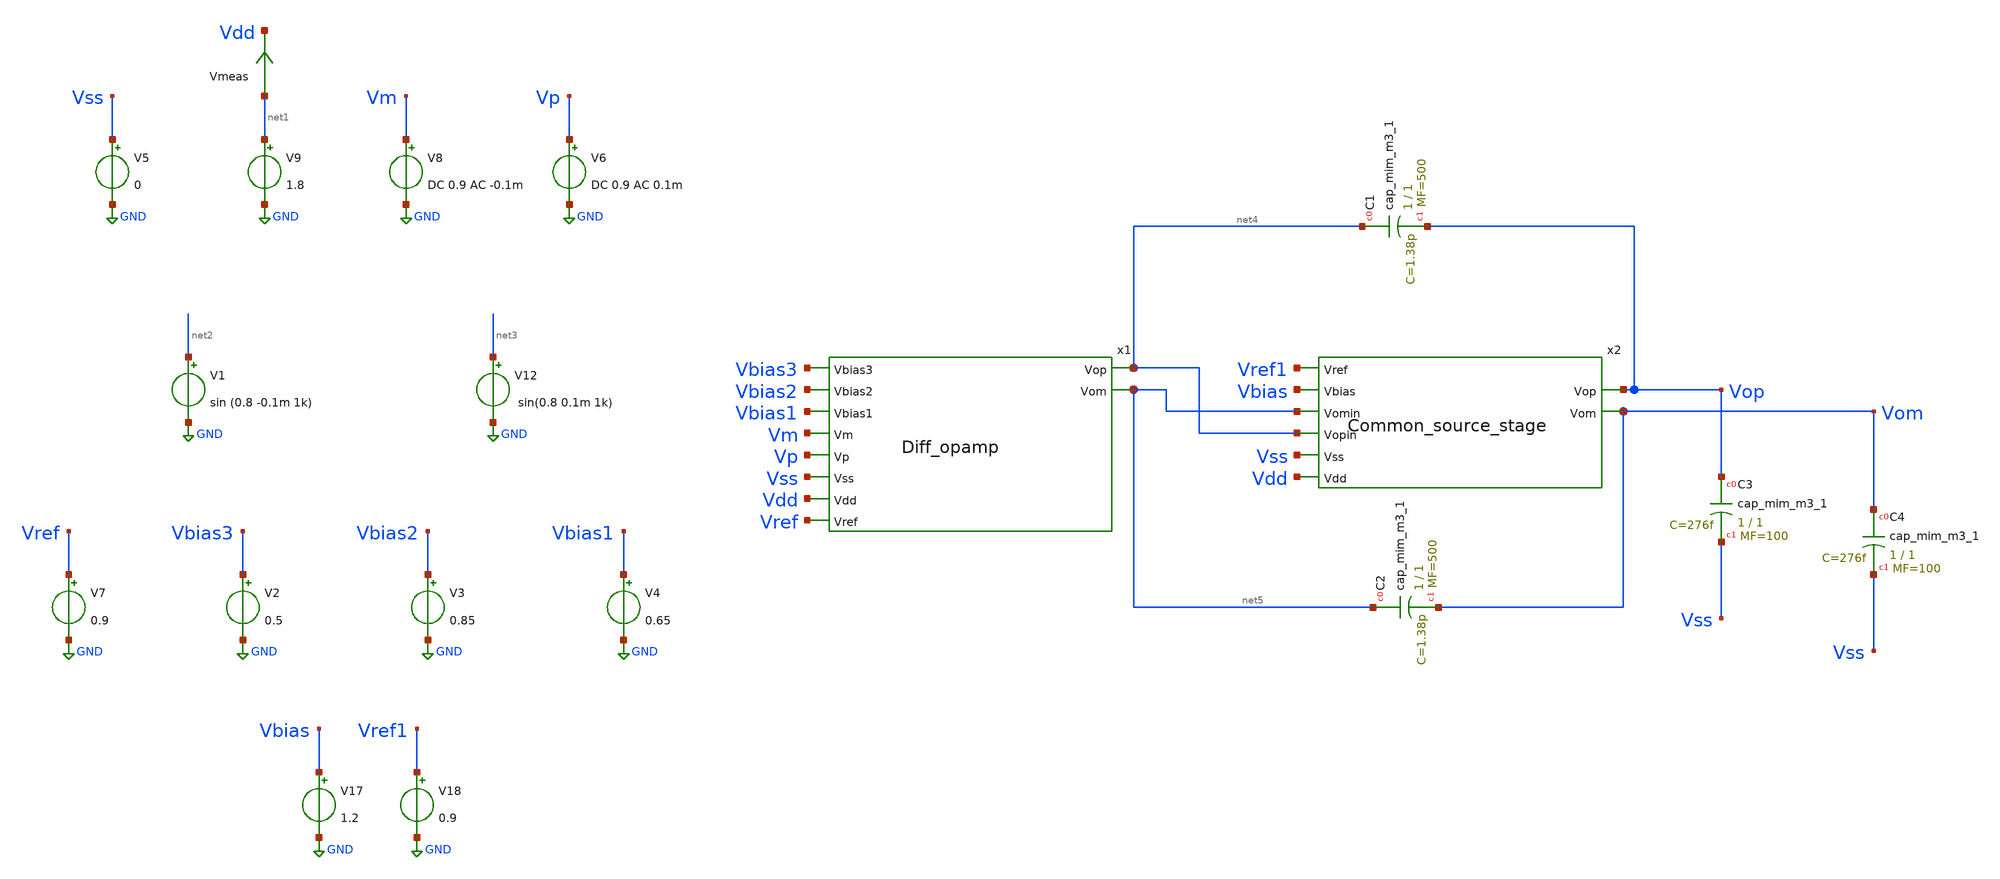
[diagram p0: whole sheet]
** sch_path: src/Opamp_Design/testbenches/OpAmp_top_tb.sch
**.subckt OpAmp_top_tb
x1 Vbias3 Vbias2 Vbias1 Vm Vp Vss Vdd Vref net4 net5 Diff_opamp
x2 Vref1 Vbias net5 net4 Vss Vdd Vop Vom Common_source_stage
V8 Vm GND DC 0.9 AC -0.1m
V6 Vp GND DC 0.9 AC 0.1m
V9 net1 GND 1.8
Vmeas net1 Vdd 0
.save i(vmeas)
V1 net2 GND sin (0.8 -0.1m 1k)
V12 net3 GND sin(0.8 0.1m 1k)
V2 Vbias3 GND 0.5
V3 Vbias2 GND 0.85
V4 Vbias1 GND 0.65
V5 Vss GND 0
V7 Vref GND 0.9
V17 Vbias GND 1.2
V18 Vref1 GND 0.9
XC1 net4 Vop sky130_fd_pr__cap_mim_m3_1 W=1 L=1 MF=500 m=500
XC3 Vop Vss sky130_fd_pr__cap_mim_m3_1 W=1 L=1 MF=100 m=100
XC4 Vom Vss sky130_fd_pr__cap_mim_m3_1 W=1 L=1 MF=100 m=100
XC2 net5 Vom sky130_fd_pr__cap_mim_m3_1 W=1 L=1 MF=500 m=500
**** begin user architecture code

** opencircuitdesign pdks install
.lib $::SKYWATER_MODELS/sky130.lib.spice tt


**** end user architecture code
**.ends

* expanding   symbol:  /foss/designs/FYP/Sky130_Multiplier/Opamp_Design/src/Diff_opamp.sym # of
*+ pins=10
** sym_path: src/Opamp_Design/src/Diff_opamp.sym
** sch_path: src/Opamp_Design/src/Diff_opamp.sch
.subckt Diff_opamp Vbias3 Vbias2 Vbias1 Vm Vp Vss Vdd Vref Vop Vom
*.ipin Vss
*.opin Vop
*.ipin Vdd
*.ipin Vp
*.ipin Vm
*.ipin Vref
*.opin Vom
*.ipin Vbias1
*.ipin Vbias2
*.ipin Vbias3
XM5 Vtest2 Vm net2 Vss sky130_fd_pr__nfet_01v8_lvt L=4 W=4 nf=1 ad='int((nf+1)/2) * W/nf * 0.29' as='int((nf+2)/2) * W/nf * 0.29'
+ pd='2*int((nf+1)/2) * (W/nf + 0.29)' ps='2*int((nf+2)/2) * (W/nf + 0.29)' nrd='0.29 / W' nrs='0.29 / W'
+ sa=0 sb=0 sd=0 mult=2 m=2
XM6 net1 Vp net2 Vss sky130_fd_pr__nfet_01v8_lvt L=4 W=4 nf=1 ad='int((nf+1)/2) * W/nf * 0.29' as='int((nf+2)/2) * W/nf * 0.29'
+ pd='2*int((nf+1)/2) * (W/nf + 0.29)' ps='2*int((nf+2)/2) * (W/nf + 0.29)' nrd='0.29 / W' nrs='0.29 / W'
+ sa=0 sb=0 sd=0 mult=2 m=2
XM11 Vop Vbias Vtest2 Vdd sky130_fd_pr__pfet_01v8_lvt L=5 W=2 nf=1 ad='int((nf+1)/2) * W/nf * 0.29' as='int((nf+2)/2) * W/nf * 0.29'
+ pd='2*int((nf+1)/2) * (W/nf + 0.29)' ps='2*int((nf+2)/2) * (W/nf + 0.29)' nrd='0.29 / W' nrs='0.29 / W'
+ sa=0 sb=0 sd=0 mult=2 m=2
XM12 Vom Vbias net1 Vdd sky130_fd_pr__pfet_01v8_lvt L=5 W=2 nf=1 ad='int((nf+1)/2) * W/nf * 0.29' as='int((nf+2)/2) * W/nf * 0.29'
+ pd='2*int((nf+1)/2) * (W/nf + 0.29)' ps='2*int((nf+2)/2) * (W/nf + 0.29)' nrd='0.29 / W' nrs='0.29 / W'
+ sa=0 sb=0 sd=0 mult=2 m=2
XM13 Vtest2 Vout Vdd Vdd sky130_fd_pr__pfet_01v8_lvt L=5 W=2 nf=1 ad='int((nf+1)/2) * W/nf * 0.29' as='int((nf+2)/2) * W/nf * 0.29'
+ pd='2*int((nf+1)/2) * (W/nf + 0.29)' ps='2*int((nf+2)/2) * (W/nf + 0.29)' nrd='0.29 / W' nrs='0.29 / W'
+ sa=0 sb=0 sd=0 mult=4 m=4
XM14 net1 Vout Vdd Vdd sky130_fd_pr__pfet_01v8_lvt L=5 W=2 nf=1 ad='int((nf+1)/2) * W/nf * 0.29' as='int((nf+2)/2) * W/nf * 0.29'
+ pd='2*int((nf+1)/2) * (W/nf + 0.29)' ps='2*int((nf+2)/2) * (W/nf + 0.29)' nrd='0.29 / W' nrs='0.29 / W'
+ sa=0 sb=0 sd=0 mult=4 m=4
XM19 net2 Vbias2 net3 Vss sky130_fd_pr__nfet_01v8_lvt L=1 W=1 nf=1 ad='int((nf+1)/2) * W/nf * 0.29' as='int((nf+2)/2) * W/nf * 0.29'
+ pd='2*int((nf+1)/2) * (W/nf + 0.29)' ps='2*int((nf+2)/2) * (W/nf + 0.29)' nrd='0.29 / W' nrs='0.29 / W'
+ sa=0 sb=0 sd=0 mult=2 m=2
XM1 net3 Vbias1 Vss Vss sky130_fd_pr__nfet_01v8_lvt L=10 W=1 nf=1 ad='int((nf+1)/2) * W/nf * 0.29' as='int((nf+2)/2) * W/nf * 0.29'
+ pd='2*int((nf+1)/2) * (W/nf + 0.29)' ps='2*int((nf+2)/2) * (W/nf + 0.29)' nrd='0.29 / W' nrs='0.29 / W'
+ sa=0 sb=0 sd=0 mult=2 m=2
XM2 net4 Vbias1 Vss Vss sky130_fd_pr__nfet_01v8_lvt L=10 W=1 nf=1 ad='int((nf+1)/2) * W/nf * 0.29' as='int((nf+2)/2) * W/nf * 0.29'
+ pd='2*int((nf+1)/2) * (W/nf + 0.29)' ps='2*int((nf+2)/2) * (W/nf + 0.29)' nrd='0.29 / W' nrs='0.29 / W'
+ sa=0 sb=0 sd=0 mult=2 m=2
XM3 net2 Vbias2 net4 Vss sky130_fd_pr__nfet_01v8_lvt L=1 W=1 nf=1 ad='int((nf+1)/2) * W/nf * 0.29' as='int((nf+2)/2) * W/nf * 0.29'
+ pd='2*int((nf+1)/2) * (W/nf + 0.29)' ps='2*int((nf+2)/2) * (W/nf + 0.29)' nrd='0.29 / W' nrs='0.29 / W'
+ sa=0 sb=0 sd=0 mult=2 m=2
XM4 Vop Vbias2 net5 Vss sky130_fd_pr__nfet_01v8_lvt L=1 W=1 nf=1 ad='int((nf+1)/2) * W/nf * 0.29' as='int((nf+2)/2) * W/nf * 0.29'
+ pd='2*int((nf+1)/2) * (W/nf + 0.29)' ps='2*int((nf+2)/2) * (W/nf + 0.29)' nrd='0.29 / W' nrs='0.29 / W'
+ sa=0 sb=0 sd=0 mult=2 m=2
XM7 net5 Vbias1 Vss Vss sky130_fd_pr__nfet_01v8_lvt L=10 W=1 nf=1 ad='int((nf+1)/2) * W/nf * 0.29' as='int((nf+2)/2) * W/nf * 0.29'
+ pd='2*int((nf+1)/2) * (W/nf + 0.29)' ps='2*int((nf+2)/2) * (W/nf + 0.29)' nrd='0.29 / W' nrs='0.29 / W'
+ sa=0 sb=0 sd=0 mult=2 m=2
XM8 Vom Vbias2 net6 Vss sky130_fd_pr__nfet_01v8_lvt L=1 W=1 nf=1 ad='int((nf+1)/2) * W/nf * 0.29' as='int((nf+2)/2) * W/nf * 0.29'
+ pd='2*int((nf+1)/2) * (W/nf + 0.29)' ps='2*int((nf+2)/2) * (W/nf + 0.29)' nrd='0.29 / W' nrs='0.29 / W'
+ sa=0 sb=0 sd=0 mult=2 m=2
XM9 net6 Vbias1 Vss Vss sky130_fd_pr__nfet_01v8_lvt L=10 W=1 nf=1 ad='int((nf+1)/2) * W/nf * 0.29' as='int((nf+2)/2) * W/nf * 0.29'
+ pd='2*int((nf+1)/2) * (W/nf + 0.29)' ps='2*int((nf+2)/2) * (W/nf + 0.29)' nrd='0.29 / W' nrs='0.29 / W'
+ sa=0 sb=0 sd=0 mult=2 m=2
XM10 Vout Vref net8 Vss sky130_fd_pr__nfet_01v8_lvt L=20 W=5 nf=1 ad='int((nf+1)/2) * W/nf * 0.29' as='int((nf+2)/2) * W/nf * 0.29'
+ pd='2*int((nf+1)/2) * (W/nf + 0.29)' ps='2*int((nf+2)/2) * (W/nf + 0.29)' nrd='0.29 / W' nrs='0.29 / W'
+ sa=0 sb=0 sd=0 mult=2 m=2
XM17 net9 Vop net8 Vss sky130_fd_pr__nfet_01v8_lvt L=20 W=5 nf=1 ad='int((nf+1)/2) * W/nf * 0.29' as='int((nf+2)/2) * W/nf * 0.29'
+ pd='2*int((nf+1)/2) * (W/nf + 0.29)' ps='2*int((nf+2)/2) * (W/nf + 0.29)' nrd='0.29 / W' nrs='0.29 / W'
+ sa=0 sb=0 sd=0 mult=2 m=2
XM18 net9 Vom net7 Vss sky130_fd_pr__nfet_01v8_lvt L=20 W=5 nf=1 ad='int((nf+1)/2) * W/nf * 0.29' as='int((nf+2)/2) * W/nf * 0.29'
+ pd='2*int((nf+1)/2) * (W/nf + 0.29)' ps='2*int((nf+2)/2) * (W/nf + 0.29)' nrd='0.29 / W' nrs='0.29 / W'
+ sa=0 sb=0 sd=0 mult=2 m=2
XM22 net7 Vbias1 Vss Vss sky130_fd_pr__nfet_01v8_lvt L=20 W=1 nf=1 ad='int((nf+1)/2) * W/nf * 0.29' as='int((nf+2)/2) * W/nf * 0.29'
+ pd='2*int((nf+1)/2) * (W/nf + 0.29)' ps='2*int((nf+2)/2) * (W/nf + 0.29)' nrd='0.29 / W' nrs='0.29 / W'
+ sa=0 sb=0 sd=0 mult=2 m=2
XM20 net9 net9 Vdd Vdd sky130_fd_pr__pfet_01v8_lvt L=10 W=1 nf=1 ad='int((nf+1)/2) * W/nf * 0.29' as='int((nf+2)/2) * W/nf * 0.29'
+ pd='2*int((nf+1)/2) * (W/nf + 0.29)' ps='2*int((nf+2)/2) * (W/nf + 0.29)' nrd='0.29 / W' nrs='0.29 / W'
+ sa=0 sb=0 sd=0 mult=2 m=2
XM21 Vout net9 Vdd Vdd sky130_fd_pr__pfet_01v8_lvt L=10 W=1 nf=1 ad='int((nf+1)/2) * W/nf * 0.29' as='int((nf+2)/2) * W/nf * 0.29'
+ pd='2*int((nf+1)/2) * (W/nf + 0.29)' ps='2*int((nf+2)/2) * (W/nf + 0.29)' nrd='0.29 / W' nrs='0.29 / W'
+ sa=0 sb=0 sd=0 mult=2 m=2
XM15 net8 Vbias1 Vss Vss sky130_fd_pr__nfet_01v8_lvt L=20 W=1 nf=1 ad='int((nf+1)/2) * W/nf * 0.29' as='int((nf+2)/2) * W/nf * 0.29'
+ pd='2*int((nf+1)/2) * (W/nf + 0.29)' ps='2*int((nf+2)/2) * (W/nf + 0.29)' nrd='0.29 / W' nrs='0.29 / W'
+ sa=0 sb=0 sd=0 mult=2 m=2
XM16 Vout Vref net7 Vss sky130_fd_pr__nfet_01v8_lvt L=20 W=5 nf=1 ad='int((nf+1)/2) * W/nf * 0.29' as='int((nf+2)/2) * W/nf * 0.29'
+ pd='2*int((nf+1)/2) * (W/nf + 0.29)' ps='2*int((nf+2)/2) * (W/nf + 0.29)' nrd='0.29 / W' nrs='0.29 / W'
+ sa=0 sb=0 sd=0 mult=2 m=2
XM46 Vbias1 Vbias1 Vss Vss sky130_fd_pr__nfet_01v8_lvt L=2 W=1 nf=1 ad='int((nf+1)/2) * W/nf * 0.29'
+ as='int((nf+2)/2) * W/nf * 0.29' pd='2*int((nf+1)/2) * (W/nf + 0.29)' ps='2*int((nf+2)/2) * (W/nf + 0.29)'
+ nrd='0.29 / W' nrs='0.29 / W' sa=0 sb=0 sd=0 mult=2 m=2
XM47 Vbias2 Vbias2 Vss Vss sky130_fd_pr__nfet_01v8_lvt L=5 W=0.6 nf=1 ad='int((nf+1)/2) * W/nf * 0.29'
+ as='int((nf+2)/2) * W/nf * 0.29' pd='2*int((nf+1)/2) * (W/nf + 0.29)' ps='2*int((nf+2)/2) * (W/nf + 0.29)'
+ nrd='0.29 / W' nrs='0.29 / W' sa=0 sb=0 sd=0 mult=2 m=2
XM23 Vbias3 Vbias3 Vss Vss sky130_fd_pr__nfet_01v8_lvt L=1 W=0.6 nf=1 ad='int((nf+1)/2) * W/nf * 0.29'
+ as='int((nf+2)/2) * W/nf * 0.29' pd='2*int((nf+1)/2) * (W/nf + 0.29)' ps='2*int((nf+2)/2) * (W/nf + 0.29)'
+ nrd='0.29 / W' nrs='0.29 / W' sa=0 sb=0 sd=0 mult=2 m=2
XM24 Vbias Vbias3 Vss Vss sky130_fd_pr__nfet_01v8_lvt L=1 W=0.6 nf=1 ad='int((nf+1)/2) * W/nf * 0.29'
+ as='int((nf+2)/2) * W/nf * 0.29' pd='2*int((nf+1)/2) * (W/nf + 0.29)' ps='2*int((nf+2)/2) * (W/nf + 0.29)'
+ nrd='0.29 / W' nrs='0.29 / W' sa=0 sb=0 sd=0 mult=2 m=2
XM25 Vbias Vbias Vdd Vdd sky130_fd_pr__pfet_01v8_lvt L=10 W=1.5 nf=1 ad='int((nf+1)/2) * W/nf * 0.29'
+ as='int((nf+2)/2) * W/nf * 0.29' pd='2*int((nf+1)/2) * (W/nf + 0.29)' ps='2*int((nf+2)/2) * (W/nf + 0.29)'
+ nrd='0.29 / W' nrs='0.29 / W' sa=0 sb=0 sd=0 mult=2 m=2
.ends


* expanding   symbol:  /foss/designs/FYP/Sky130_Multiplier/Opamp_Design/src/Common_source_stage.sym
*+ # of pins=8
** sym_path: src/Opamp_Design/src/Common_source_stage.sym
** sch_path: src/Opamp_Design/src/Common_source_stage.sch
.subckt Common_source_stage Vref Vbias Vomin Vopin Vss Vdd Vop Vom
*.ipin Vdd
*.opin Vop
*.ipin Vss
*.opin Vom
*.ipin Vopin
*.ipin Vomin
*.ipin Vbias
*.ipin Vref
XM9 Vop Vopin Vdd Vdd sky130_fd_pr__pfet_01v8_lvt L=1 W=2 nf=1 ad='int((nf+1)/2) * W/nf * 0.29' as='int((nf+2)/2) * W/nf * 0.29'
+ pd='2*int((nf+1)/2) * (W/nf + 0.29)' ps='2*int((nf+2)/2) * (W/nf + 0.29)' nrd='0.29 / W' nrs='0.29 / W'
+ sa=0 sb=0 sd=0 mult=9 m=9
XM4 Vom Vomin Vdd Vdd sky130_fd_pr__pfet_01v8_lvt L=1 W=2 nf=1 ad='int((nf+1)/2) * W/nf * 0.29' as='int((nf+2)/2) * W/nf * 0.29'
+ pd='2*int((nf+1)/2) * (W/nf + 0.29)' ps='2*int((nf+2)/2) * (W/nf + 0.29)' nrd='0.29 / W' nrs='0.29 / W'
+ sa=0 sb=0 sd=0 mult=9 m=9
XM2 Vop Vout Vss Vss sky130_fd_pr__nfet_01v8_lvt L=1 W=1 nf=1 ad='int((nf+1)/2) * W/nf * 0.29' as='int((nf+2)/2) * W/nf * 0.29'
+ pd='2*int((nf+1)/2) * (W/nf + 0.29)' ps='2*int((nf+2)/2) * (W/nf + 0.29)' nrd='0.29 / W' nrs='0.29 / W'
+ sa=0 sb=0 sd=0 mult=9 m=9
XM1 Vom Vout Vss Vss sky130_fd_pr__nfet_01v8_lvt L=1 W=1 nf=1 ad='int((nf+1)/2) * W/nf * 0.29' as='int((nf+2)/2) * W/nf * 0.29'
+ pd='2*int((nf+1)/2) * (W/nf + 0.29)' ps='2*int((nf+2)/2) * (W/nf + 0.29)' nrd='0.29 / W' nrs='0.29 / W'
+ sa=0 sb=0 sd=0 mult=9 m=9
XM3 net1 Vbiasp Vdd Vdd sky130_fd_pr__pfet_01v8_lvt L=5 W=1 nf=1 ad='int((nf+1)/2) * W/nf * 0.29' as='int((nf+2)/2) * W/nf * 0.29'
+ pd='2*int((nf+1)/2) * (W/nf + 0.29)' ps='2*int((nf+2)/2) * (W/nf + 0.29)' nrd='0.29 / W' nrs='0.29 / W'
+ sa=0 sb=0 sd=0 mult=2 m=2
XM7 Vtest Vcm net1 Vdd sky130_fd_pr__pfet_01v8_lvt L=10 W=1 nf=1 ad='int((nf+1)/2) * W/nf * 0.29' as='int((nf+2)/2) * W/nf * 0.29'
+ pd='2*int((nf+1)/2) * (W/nf + 0.29)' ps='2*int((nf+2)/2) * (W/nf + 0.29)' nrd='0.29 / W' nrs='0.29 / W'
+ sa=0 sb=0 sd=0 mult=2 m=2
XM8 Vout Vref net1 Vdd sky130_fd_pr__pfet_01v8_lvt L=10 W=1 nf=1 ad='int((nf+1)/2) * W/nf * 0.29' as='int((nf+2)/2) * W/nf * 0.29'
+ pd='2*int((nf+1)/2) * (W/nf + 0.29)' ps='2*int((nf+2)/2) * (W/nf + 0.29)' nrd='0.29 / W' nrs='0.29 / W'
+ sa=0 sb=0 sd=0 mult=2 m=2
XM5 Vtest Vtest Vss Vss sky130_fd_pr__nfet_01v8_lvt L=20 W=0.5 nf=1 ad='int((nf+1)/2) * W/nf * 0.29'
+ as='int((nf+2)/2) * W/nf * 0.29' pd='2*int((nf+1)/2) * (W/nf + 0.29)' ps='2*int((nf+2)/2) * (W/nf + 0.29)'
+ nrd='0.29 / W' nrs='0.29 / W' sa=0 sb=0 sd=0 mult=2 m=2
XM6 Vout Vtest Vss Vss sky130_fd_pr__nfet_01v8_lvt L=20 W=0.5 nf=1 ad='int((nf+1)/2) * W/nf * 0.29' as='int((nf+2)/2) * W/nf * 0.29'
+ pd='2*int((nf+1)/2) * (W/nf + 0.29)' ps='2*int((nf+2)/2) * (W/nf + 0.29)' nrd='0.29 / W' nrs='0.29 / W'
+ sa=0 sb=0 sd=0 mult=2 m=2
x1 Vop Vcm res_pack
x2 Vcm Vom res_pack
XM10 Vbias Vbias Vss Vss sky130_fd_pr__nfet_01v8_lvt L=1 W=0.6 nf=1 ad='int((nf+1)/2) * W/nf * 0.29'
+ as='int((nf+2)/2) * W/nf * 0.29' pd='2*int((nf+1)/2) * (W/nf + 0.29)' ps='2*int((nf+2)/2) * (W/nf + 0.29)'
+ nrd='0.29 / W' nrs='0.29 / W' sa=0 sb=0 sd=0 mult=2 m=2
XM11 Vbiasp Vbias Vss Vss sky130_fd_pr__nfet_01v8_lvt L=1 W=0.6 nf=1 ad='int((nf+1)/2) * W/nf * 0.29'
+ as='int((nf+2)/2) * W/nf * 0.29' pd='2*int((nf+1)/2) * (W/nf + 0.29)' ps='2*int((nf+2)/2) * (W/nf + 0.29)'
+ nrd='0.29 / W' nrs='0.29 / W' sa=0 sb=0 sd=0 mult=2 m=2
XM12 Vbiasp Vbiasp Vdd Vdd sky130_fd_pr__pfet_01v8_lvt L=1 W=6 nf=1 ad='int((nf+1)/2) * W/nf * 0.29'
+ as='int((nf+2)/2) * W/nf * 0.29' pd='2*int((nf+1)/2) * (W/nf + 0.29)' ps='2*int((nf+2)/2) * (W/nf + 0.29)'
+ nrd='0.29 / W' nrs='0.29 / W' sa=0 sb=0 sd=0 mult=2 m=2
.ends


* expanding   symbol:  /foss/designs/FYP/Sky130_Design/Opamp_Design/src/res_pack.sym # of pins=2
** sym_path: src/Opamp_Design/src/res_pack.sym
** sch_path: src/Opamp_Design/src/res_pack.sch
.subckt res_pack Vin Vout
*.ipin Vin
*.opin Vout
XR1 net4 Vin sky130_fd_pr__res_generic_po W=0.5 L=40 m=1
XR2 net5 net4 sky130_fd_pr__res_generic_po W=0.5 L=40 m=1
XR3 net6 net5 sky130_fd_pr__res_generic_po W=0.5 L=40 m=1
XR4 net7 net6 sky130_fd_pr__res_generic_po W=0.5 L=40 m=1
XR5 net1 net7 sky130_fd_pr__res_generic_po W=0.5 L=40 m=1
XR6 net8 net2 sky130_fd_pr__res_generic_po W=0.5 L=40 m=1
XR7 net9 net8 sky130_fd_pr__res_generic_po W=0.5 L=40 m=1
XR8 net10 net9 sky130_fd_pr__res_generic_po W=0.5 L=40 m=1
XR9 net11 net10 sky130_fd_pr__res_generic_po W=0.5 L=40 m=1
XR10 net1 net11 sky130_fd_pr__res_generic_po W=0.5 L=40 m=1
XR11 net12 net2 sky130_fd_pr__res_generic_po W=0.5 L=40 m=1
XR12 net13 net12 sky130_fd_pr__res_generic_po W=0.5 L=40 m=1
XR13 net14 net13 sky130_fd_pr__res_generic_po W=0.5 L=40 m=1
XR14 net15 net14 sky130_fd_pr__res_generic_po W=0.5 L=40 m=1
XR16 net16 Vout sky130_fd_pr__res_generic_po W=0.5 L=40 m=1
XR17 net17 net16 sky130_fd_pr__res_generic_po W=0.5 L=40 m=1
XR18 net18 net17 sky130_fd_pr__res_generic_po W=0.5 L=40 m=1
XR19 net19 net18 sky130_fd_pr__res_generic_po W=0.5 L=40 m=1
XR20 net3 net19 sky130_fd_pr__res_generic_po W=0.5 L=40 m=1
XR15 net3 net15 sky130_fd_pr__res_generic_po W=0.5 L=40 m=1
.ends

.GLOBAL GND
**** begin user architecture code



* ngspice commands
.options savecurrents

.control
save all
save @m.x1.xm5.msky130_fd_pr__nfet_01v8_lvt[gm]
save @m.x1.xm1.msky130_fd_pr__nfet_01v8_lvt[gm]
save @m.x1.xm2.msky130_fd_pr__nfet_01v8_lvt[gm]
save @m.x1.xm3.msky130_fd_pr__nfet_01v8_lvt[gm]
save @m.x1.xm4.msky130_fd_pr__nfet_01v8_lvt[gm]
save @m.x1.xm6.msky130_fd_pr__nfet_01v8_lvt[gm]
save @m.x1.xm7.msky130_fd_pr__nfet_01v8_lvt[gm]
save @m.x1.xm8.msky130_fd_pr__nfet_01v8_lvt[gm]
save @m.x1.xm9.msky130_fd_pr__nfet_01v8_lvt[gm]
save @m.x1.xm10.msky130_fd_pr__nfet_01v8_lvt[gm]
save @m.x1.xm11.msky130_fd_pr__pfet_01v8_lvt[gm]
save @m.x1.xm12.msky130_fd_pr__pfet_01v8_lvt[gm]
save @m.x1.xm13.msky130_fd_pr__pfet_01v8_lvt[gm]
save @m.x1.xm14.msky130_fd_pr__pfet_01v8_lvt[gm]
save @m.x1.xm15.msky130_fd_pr__nfet_01v8_lvt[gm]
save @m.x1.xm16.msky130_fd_pr__nfet_01v8_lvt[gm]
save @m.x1.xm17.msky130_fd_pr__nfet_01v8_lvt[gm]
save @m.x1.xm18.msky130_fd_pr__nfet_01v8_lvt[gm]
save @m.x1.xm19.msky130_fd_pr__nfet_01v8_lvt[gm]
save @m.x1.xm20.msky130_fd_pr__pfet_01v8_lvt[gm]
save @m.x1.xm21.msky130_fd_pr__pfet_01v8_lvt[gm]
save @m.x1.xm22.msky130_fd_pr__nfet_01v8_lvt[gm]

save @m.x2.xm1.msky130_fd_pr__nfet_01v8_lvt[gm]
save @m.x2.xm2.msky130_fd_pr__nfet_01v8_lvt[gm]
save @m.x2.xm3.msky130_fd_pr__pfet_01v8_lvt[gm]
save @m.x2.xm4.msky130_fd_pr__pfet_01v8_lvt[gm]
save @m.x2.xm5.msky130_fd_pr__nfet_01v8_lvt[gm]
save @m.x2.xm6.msky130_fd_pr__nfet_01v8_lvt[gm]
save @m.x2.xm7.msky130_fd_pr__pfet_01v8_lvt[gm]
save @m.x2.xm8.msky130_fd_pr__pfet_01v8_lvt[gm]
save @m.x2.xm9.msky130_fd_pr__pfet_01v8_lvt[gm]

save @m.x1.xm5.msky130_fd_pr__nfet_01v8_lvt[vth]
save @m.x1.xm1.msky130_fd_pr__nfet_01v8_lvt[vth]
save @m.x1.xm2.msky130_fd_pr__nfet_01v8_lvt[vth]
save @m.x1.xm3.msky130_fd_pr__nfet_01v8_lvt[vth]
save @m.x1.xm4.msky130_fd_pr__nfet_01v8_lvt[vth]
save @m.x1.xm6.msky130_fd_pr__nfet_01v8_lvt[vth]
save @m.x1.xm7.msky130_fd_pr__nfet_01v8_lvt[vth]
save @m.x1.xm8.msky130_fd_pr__nfet_01v8_lvt[vth]
save @m.x1.xm9.msky130_fd_pr__nfet_01v8_lvt[vth]
save @m.x1.xm10.msky130_fd_pr__nfet_01v8_lvt[vth]
save @m.x1.xm11.msky130_fd_pr__pfet_01v8_lvt[vth]
save @m.x1.xm12.msky130_fd_pr__pfet_01v8_lvt[vth]
save @m.x1.xm13.msky130_fd_pr__pfet_01v8_lvt[vth]
save @m.x1.xm14.msky130_fd_pr__pfet_01v8_lvt[vth]
save @m.x1.xm15.msky130_fd_pr__nfet_01v8_lvt[vth]
save @m.x1.xm16.msky130_fd_pr__nfet_01v8_lvt[vth]
save @m.x1.xm17.msky130_fd_pr__nfet_01v8_lvt[vth]
save @m.x1.xm18.msky130_fd_pr__nfet_01v8_lvt[vth]
save @m.x1.xm19.msky130_fd_pr__nfet_01v8_lvt[vth]
save @m.x1.xm20.msky130_fd_pr__pfet_01v8_lvt[vth]
save @m.x1.xm21.msky130_fd_pr__pfet_01v8_lvt[vth]
save @m.x1.xm22.msky130_fd_pr__nfet_01v8_lvt[vth]

save @m.x2.xm1.msky130_fd_pr__nfet_01v8_lvt[vth]
save @m.x2.xm2.msky130_fd_pr__nfet_01v8_lvt[vth]
save @m.x2.xm3.msky130_fd_pr__pfet_01v8_lvt[vth]
save @m.x2.xm4.msky130_fd_pr__pfet_01v8_lvt[vth]
save @m.x2.xm5.msky130_fd_pr__nfet_01v8_lvt[vth]
save @m.x2.xm6.msky130_fd_pr__nfet_01v8_lvt[vth]
save @m.x2.xm7.msky130_fd_pr__pfet_01v8_lvt[vth]
save @m.x2.xm8.msky130_fd_pr__pfet_01v8_lvt[vth]
save @m.x2.xm9.msky130_fd_pr__pfet_01v8_lvt[vth]


op
ac dec 101 1 10000MEG
*tran 100u 100m
let vdiff = v(Vop)-v(Vom)
let vin = v(Vp) - v(Vm)
plot db(vdiff/vin) (180/pi)*phase(vdiff/vin)
write Opamp_top_tb.raw
.endc



**** end user architecture code
.end
